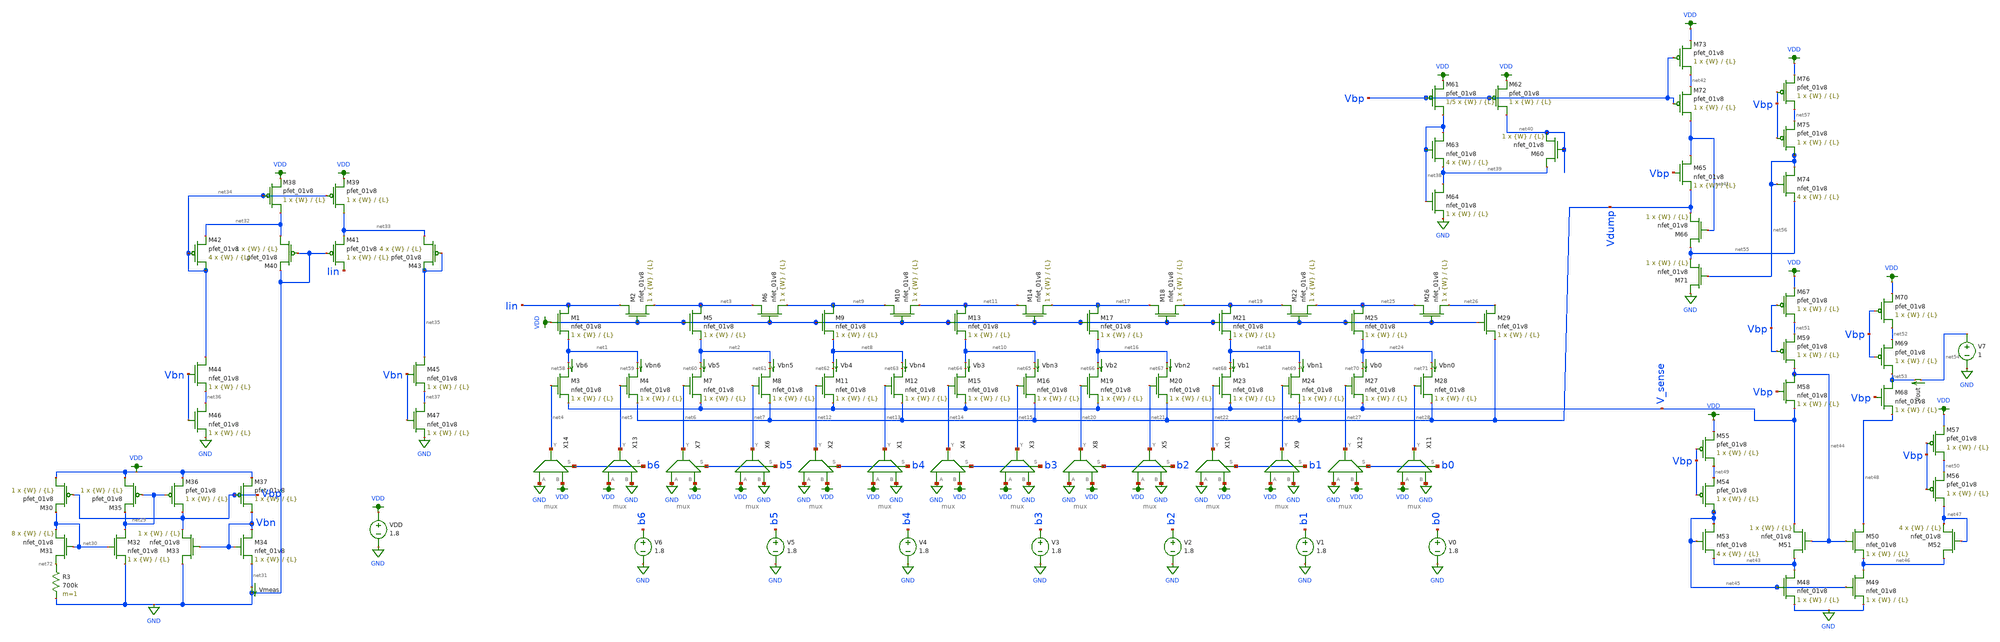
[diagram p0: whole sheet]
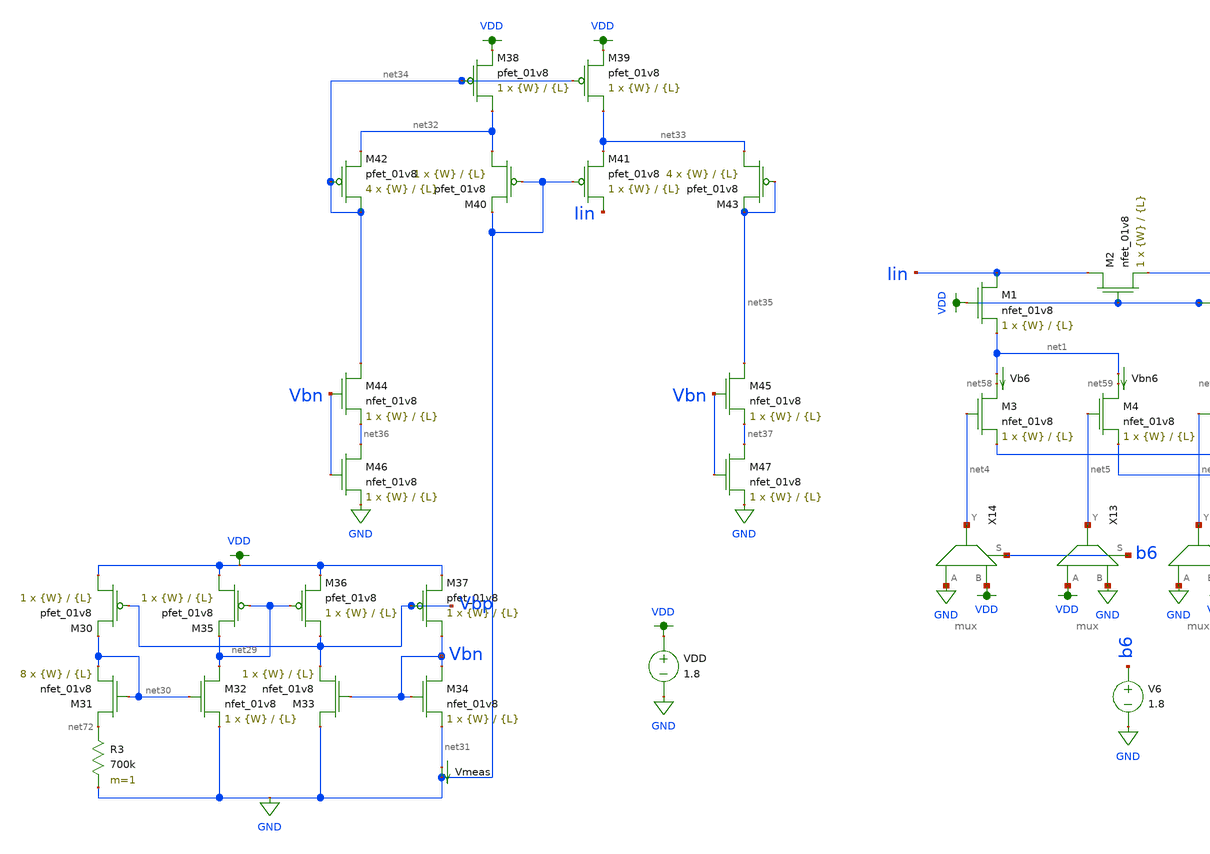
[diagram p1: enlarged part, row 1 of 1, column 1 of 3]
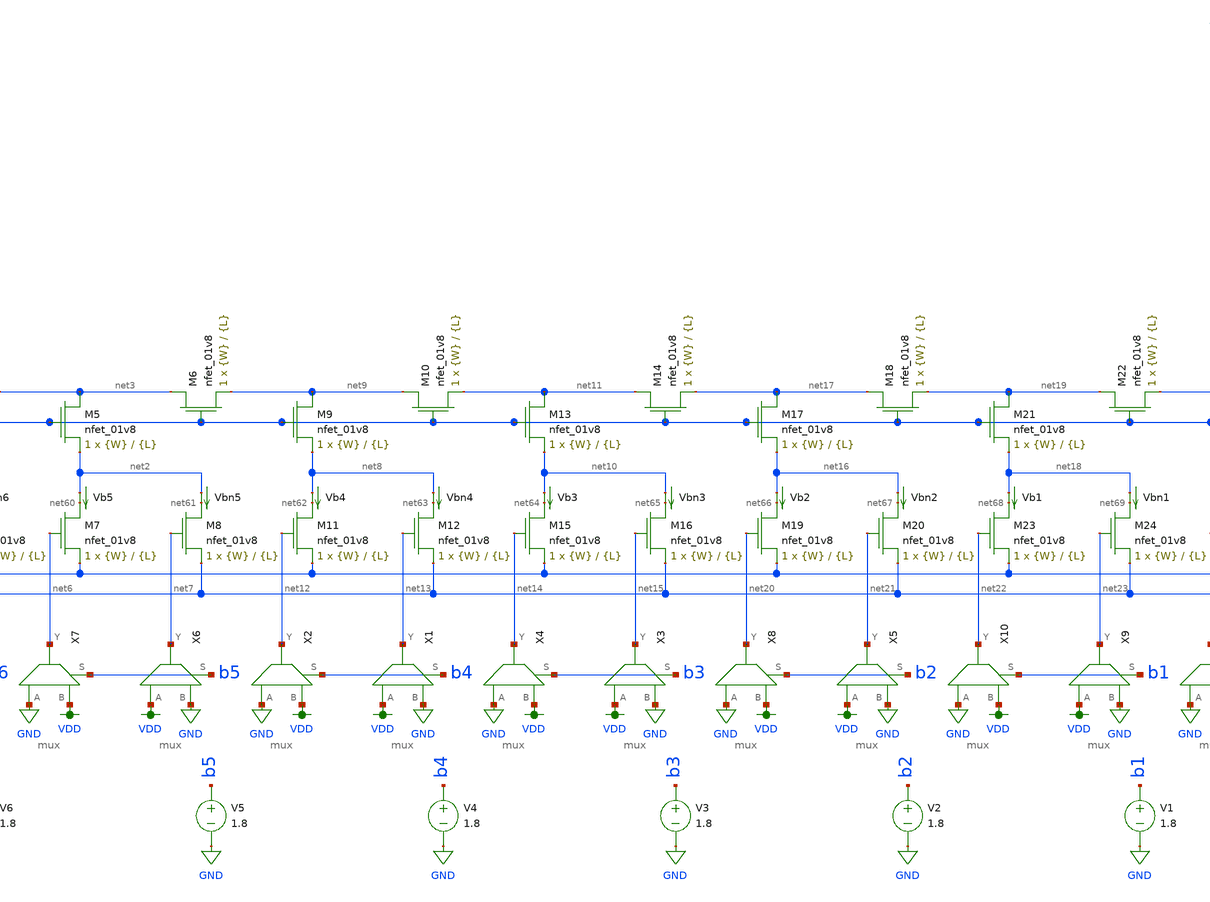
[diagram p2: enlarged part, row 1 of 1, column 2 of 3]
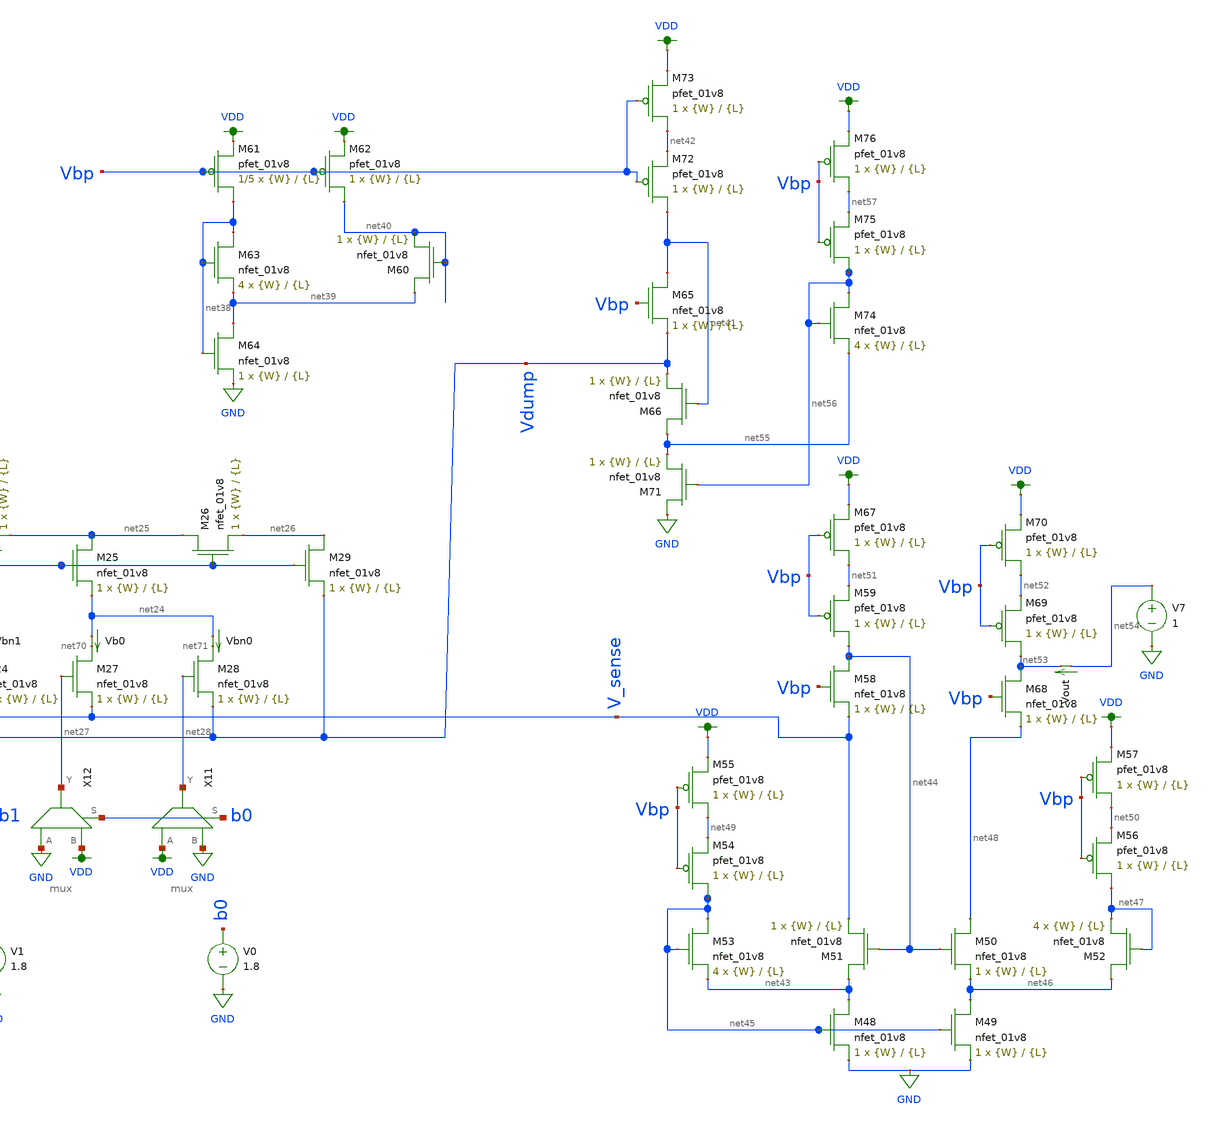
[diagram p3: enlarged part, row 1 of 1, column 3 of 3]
** sch_path: dac/schematics/misc/dac_from_paper.sch
**.subckt dac_from_paper
XM1 Iin VDD net1 GND sky130_fd_pr__nfet_01v8 L={L} W={W} nf=1 ad='int((nf+1)/2) * W/nf * 0.29' as='int((nf+2)/2) * W/nf * 0.29'
+ pd='2*int((nf+1)/2) * (W/nf + 0.29)' ps='2*int((nf+2)/2) * (W/nf + 0.29)' nrd='0.29 / W' nrs='0.29 / W'
+ sa=0 sb=0 sd=0 mult=1 m=1
XM2 Iin VDD net3 GND sky130_fd_pr__nfet_01v8 L={L} W={W} nf=1 ad='int((nf+1)/2) * W/nf * 0.29' as='int((nf+2)/2) * W/nf * 0.29'
+ pd='2*int((nf+1)/2) * (W/nf + 0.29)' ps='2*int((nf+2)/2) * (W/nf + 0.29)' nrd='0.29 / W' nrs='0.29 / W'
+ sa=0 sb=0 sd=0 mult=1 m=1
XM3 net58 net4 V_sense GND sky130_fd_pr__nfet_01v8 L={L} W={W} nf=1 ad='int((nf+1)/2) * W/nf * 0.29'
+ as='int((nf+2)/2) * W/nf * 0.29' pd='2*int((nf+1)/2) * (W/nf + 0.29)' ps='2*int((nf+2)/2) * (W/nf + 0.29)'
+ nrd='0.29 / W' nrs='0.29 / W' sa=0 sb=0 sd=0 mult=1 m=1
XM4 net59 net5 Vdump GND sky130_fd_pr__nfet_01v8 L={L} W={W} nf=1 ad='int((nf+1)/2) * W/nf * 0.29' as='int((nf+2)/2) * W/nf * 0.29'
+ pd='2*int((nf+1)/2) * (W/nf + 0.29)' ps='2*int((nf+2)/2) * (W/nf + 0.29)' nrd='0.29 / W' nrs='0.29 / W'
+ sa=0 sb=0 sd=0 mult=1 m=1
XM5 net3 VDD net2 GND sky130_fd_pr__nfet_01v8 L={L} W={W} nf=1 ad='int((nf+1)/2) * W/nf * 0.29' as='int((nf+2)/2) * W/nf * 0.29'
+ pd='2*int((nf+1)/2) * (W/nf + 0.29)' ps='2*int((nf+2)/2) * (W/nf + 0.29)' nrd='0.29 / W' nrs='0.29 / W'
+ sa=0 sb=0 sd=0 mult=1 m=1
XM6 net3 VDD net9 GND sky130_fd_pr__nfet_01v8 L={L} W={W} nf=1 ad='int((nf+1)/2) * W/nf * 0.29' as='int((nf+2)/2) * W/nf * 0.29'
+ pd='2*int((nf+1)/2) * (W/nf + 0.29)' ps='2*int((nf+2)/2) * (W/nf + 0.29)' nrd='0.29 / W' nrs='0.29 / W'
+ sa=0 sb=0 sd=0 mult=1 m=1
XM7 net60 net6 V_sense GND sky130_fd_pr__nfet_01v8 L={L} W={W} nf=1 ad='int((nf+1)/2) * W/nf * 0.29'
+ as='int((nf+2)/2) * W/nf * 0.29' pd='2*int((nf+1)/2) * (W/nf + 0.29)' ps='2*int((nf+2)/2) * (W/nf + 0.29)'
+ nrd='0.29 / W' nrs='0.29 / W' sa=0 sb=0 sd=0 mult=1 m=1
XM8 net61 net7 Vdump GND sky130_fd_pr__nfet_01v8 L={L} W={W} nf=1 ad='int((nf+1)/2) * W/nf * 0.29' as='int((nf+2)/2) * W/nf * 0.29'
+ pd='2*int((nf+1)/2) * (W/nf + 0.29)' ps='2*int((nf+2)/2) * (W/nf + 0.29)' nrd='0.29 / W' nrs='0.29 / W'
+ sa=0 sb=0 sd=0 mult=1 m=1
XM9 net9 VDD net8 GND sky130_fd_pr__nfet_01v8 L={L} W={W} nf=1 ad='int((nf+1)/2) * W/nf * 0.29' as='int((nf+2)/2) * W/nf * 0.29'
+ pd='2*int((nf+1)/2) * (W/nf + 0.29)' ps='2*int((nf+2)/2) * (W/nf + 0.29)' nrd='0.29 / W' nrs='0.29 / W'
+ sa=0 sb=0 sd=0 mult=1 m=1
XM10 net9 VDD net11 GND sky130_fd_pr__nfet_01v8 L={L} W={W} nf=1 ad='int((nf+1)/2) * W/nf * 0.29' as='int((nf+2)/2) * W/nf * 0.29'
+ pd='2*int((nf+1)/2) * (W/nf + 0.29)' ps='2*int((nf+2)/2) * (W/nf + 0.29)' nrd='0.29 / W' nrs='0.29 / W'
+ sa=0 sb=0 sd=0 mult=1 m=1
XM11 net62 net12 V_sense GND sky130_fd_pr__nfet_01v8 L={L} W={W} nf=1 ad='int((nf+1)/2) * W/nf * 0.29'
+ as='int((nf+2)/2) * W/nf * 0.29' pd='2*int((nf+1)/2) * (W/nf + 0.29)' ps='2*int((nf+2)/2) * (W/nf + 0.29)'
+ nrd='0.29 / W' nrs='0.29 / W' sa=0 sb=0 sd=0 mult=1 m=1
XM12 net63 net13 Vdump GND sky130_fd_pr__nfet_01v8 L={L} W={W} nf=1 ad='int((nf+1)/2) * W/nf * 0.29'
+ as='int((nf+2)/2) * W/nf * 0.29' pd='2*int((nf+1)/2) * (W/nf + 0.29)' ps='2*int((nf+2)/2) * (W/nf + 0.29)'
+ nrd='0.29 / W' nrs='0.29 / W' sa=0 sb=0 sd=0 mult=1 m=1
XM13 net11 VDD net10 GND sky130_fd_pr__nfet_01v8 L={L} W={W} nf=1 ad='int((nf+1)/2) * W/nf * 0.29' as='int((nf+2)/2) * W/nf * 0.29'
+ pd='2*int((nf+1)/2) * (W/nf + 0.29)' ps='2*int((nf+2)/2) * (W/nf + 0.29)' nrd='0.29 / W' nrs='0.29 / W'
+ sa=0 sb=0 sd=0 mult=1 m=1
XM14 net11 VDD net17 GND sky130_fd_pr__nfet_01v8 L={L} W={W} nf=1 ad='int((nf+1)/2) * W/nf * 0.29' as='int((nf+2)/2) * W/nf * 0.29'
+ pd='2*int((nf+1)/2) * (W/nf + 0.29)' ps='2*int((nf+2)/2) * (W/nf + 0.29)' nrd='0.29 / W' nrs='0.29 / W'
+ sa=0 sb=0 sd=0 mult=1 m=1
XM15 net64 net14 V_sense GND sky130_fd_pr__nfet_01v8 L={L} W={W} nf=1 ad='int((nf+1)/2) * W/nf * 0.29'
+ as='int((nf+2)/2) * W/nf * 0.29' pd='2*int((nf+1)/2) * (W/nf + 0.29)' ps='2*int((nf+2)/2) * (W/nf + 0.29)'
+ nrd='0.29 / W' nrs='0.29 / W' sa=0 sb=0 sd=0 mult=1 m=1
XM16 net65 net15 Vdump GND sky130_fd_pr__nfet_01v8 L={L} W={W} nf=1 ad='int((nf+1)/2) * W/nf * 0.29'
+ as='int((nf+2)/2) * W/nf * 0.29' pd='2*int((nf+1)/2) * (W/nf + 0.29)' ps='2*int((nf+2)/2) * (W/nf + 0.29)'
+ nrd='0.29 / W' nrs='0.29 / W' sa=0 sb=0 sd=0 mult=1 m=1
XM17 net17 VDD net16 GND sky130_fd_pr__nfet_01v8 L={L} W={W} nf=1 ad='int((nf+1)/2) * W/nf * 0.29' as='int((nf+2)/2) * W/nf * 0.29'
+ pd='2*int((nf+1)/2) * (W/nf + 0.29)' ps='2*int((nf+2)/2) * (W/nf + 0.29)' nrd='0.29 / W' nrs='0.29 / W'
+ sa=0 sb=0 sd=0 mult=1 m=1
XM18 net17 VDD net19 GND sky130_fd_pr__nfet_01v8 L={L} W={W} nf=1 ad='int((nf+1)/2) * W/nf * 0.29' as='int((nf+2)/2) * W/nf * 0.29'
+ pd='2*int((nf+1)/2) * (W/nf + 0.29)' ps='2*int((nf+2)/2) * (W/nf + 0.29)' nrd='0.29 / W' nrs='0.29 / W'
+ sa=0 sb=0 sd=0 mult=1 m=1
XM19 net66 net20 V_sense GND sky130_fd_pr__nfet_01v8 L={L} W={W} nf=1 ad='int((nf+1)/2) * W/nf * 0.29'
+ as='int((nf+2)/2) * W/nf * 0.29' pd='2*int((nf+1)/2) * (W/nf + 0.29)' ps='2*int((nf+2)/2) * (W/nf + 0.29)'
+ nrd='0.29 / W' nrs='0.29 / W' sa=0 sb=0 sd=0 mult=1 m=1
XM20 net67 net21 Vdump GND sky130_fd_pr__nfet_01v8 L={L} W={W} nf=1 ad='int((nf+1)/2) * W/nf * 0.29'
+ as='int((nf+2)/2) * W/nf * 0.29' pd='2*int((nf+1)/2) * (W/nf + 0.29)' ps='2*int((nf+2)/2) * (W/nf + 0.29)'
+ nrd='0.29 / W' nrs='0.29 / W' sa=0 sb=0 sd=0 mult=1 m=1
XM21 net19 VDD net18 GND sky130_fd_pr__nfet_01v8 L={L} W={W} nf=1 ad='int((nf+1)/2) * W/nf * 0.29' as='int((nf+2)/2) * W/nf * 0.29'
+ pd='2*int((nf+1)/2) * (W/nf + 0.29)' ps='2*int((nf+2)/2) * (W/nf + 0.29)' nrd='0.29 / W' nrs='0.29 / W'
+ sa=0 sb=0 sd=0 mult=1 m=1
XM22 net19 VDD net25 GND sky130_fd_pr__nfet_01v8 L={L} W={W} nf=1 ad='int((nf+1)/2) * W/nf * 0.29' as='int((nf+2)/2) * W/nf * 0.29'
+ pd='2*int((nf+1)/2) * (W/nf + 0.29)' ps='2*int((nf+2)/2) * (W/nf + 0.29)' nrd='0.29 / W' nrs='0.29 / W'
+ sa=0 sb=0 sd=0 mult=1 m=1
XM23 net68 net22 V_sense GND sky130_fd_pr__nfet_01v8 L={L} W={W} nf=1 ad='int((nf+1)/2) * W/nf * 0.29'
+ as='int((nf+2)/2) * W/nf * 0.29' pd='2*int((nf+1)/2) * (W/nf + 0.29)' ps='2*int((nf+2)/2) * (W/nf + 0.29)'
+ nrd='0.29 / W' nrs='0.29 / W' sa=0 sb=0 sd=0 mult=1 m=1
XM24 net69 net23 Vdump GND sky130_fd_pr__nfet_01v8 L={L} W={W} nf=1 ad='int((nf+1)/2) * W/nf * 0.29'
+ as='int((nf+2)/2) * W/nf * 0.29' pd='2*int((nf+1)/2) * (W/nf + 0.29)' ps='2*int((nf+2)/2) * (W/nf + 0.29)'
+ nrd='0.29 / W' nrs='0.29 / W' sa=0 sb=0 sd=0 mult=1 m=1
XM25 net25 VDD net24 GND sky130_fd_pr__nfet_01v8 L={L} W={W} nf=1 ad='int((nf+1)/2) * W/nf * 0.29' as='int((nf+2)/2) * W/nf * 0.29'
+ pd='2*int((nf+1)/2) * (W/nf + 0.29)' ps='2*int((nf+2)/2) * (W/nf + 0.29)' nrd='0.29 / W' nrs='0.29 / W'
+ sa=0 sb=0 sd=0 mult=1 m=1
XM26 net25 VDD net26 GND sky130_fd_pr__nfet_01v8 L={L} W={W} nf=1 ad='int((nf+1)/2) * W/nf * 0.29' as='int((nf+2)/2) * W/nf * 0.29'
+ pd='2*int((nf+1)/2) * (W/nf + 0.29)' ps='2*int((nf+2)/2) * (W/nf + 0.29)' nrd='0.29 / W' nrs='0.29 / W'
+ sa=0 sb=0 sd=0 mult=1 m=1
XM27 net70 net27 V_sense GND sky130_fd_pr__nfet_01v8 L={L} W={W} nf=1 ad='int((nf+1)/2) * W/nf * 0.29'
+ as='int((nf+2)/2) * W/nf * 0.29' pd='2*int((nf+1)/2) * (W/nf + 0.29)' ps='2*int((nf+2)/2) * (W/nf + 0.29)'
+ nrd='0.29 / W' nrs='0.29 / W' sa=0 sb=0 sd=0 mult=1 m=1
XM28 net71 net28 Vdump GND sky130_fd_pr__nfet_01v8 L={L} W={W} nf=1 ad='int((nf+1)/2) * W/nf * 0.29'
+ as='int((nf+2)/2) * W/nf * 0.29' pd='2*int((nf+1)/2) * (W/nf + 0.29)' ps='2*int((nf+2)/2) * (W/nf + 0.29)'
+ nrd='0.29 / W' nrs='0.29 / W' sa=0 sb=0 sd=0 mult=1 m=1
XM29 net26 VDD Vdump GND sky130_fd_pr__nfet_01v8 L={L} W={W} nf=1 ad='int((nf+1)/2) * W/nf * 0.29' as='int((nf+2)/2) * W/nf * 0.29'
+ pd='2*int((nf+1)/2) * (W/nf + 0.29)' ps='2*int((nf+2)/2) * (W/nf + 0.29)' nrd='0.29 / W' nrs='0.29 / W'
+ sa=0 sb=0 sd=0 mult=1 m=1
Vb0 net24 net70 0
.save i(vb0)
Vbn0 net24 net71 0
.save i(vbn0)
Vb5 net2 net60 0
.save i(vb5)
Vb6 net1 net58 0
.save i(vb6)
Vb1 net18 net68 0
.save i(vb1)
Vb2 net16 net66 0
.save i(vb2)
Vb3 net10 net64 0
.save i(vb3)
Vb4 net8 net62 0
.save i(vb4)
Vbn1 net18 net69 0
.save i(vbn1)
Vbn2 net16 net67 0
.save i(vbn2)
Vbn3 net10 net65 0
.save i(vbn3)
Vbn4 net8 net63 0
.save i(vbn4)
Vbn5 net2 net61 0
.save i(vbn5)
Vbn6 net1 net59 0
.save i(vbn6)
V0 b0 GND 1.8
V1 b1 GND 1.8
V2 b2 GND 1.8
V3 b3 GND 1.8
V4 b4 GND 1.8
V5 b5 GND 1.8
V6 b6 GND 1.8
XM30 VDD Vbp net30 VDD sky130_fd_pr__pfet_01v8 L={L} W={W} nf=1 ad='int((nf+1)/2) * W/nf * 0.29' as='int((nf+2)/2) * W/nf * 0.29'
+ pd='2*int((nf+1)/2) * (W/nf + 0.29)' ps='2*int((nf+2)/2) * (W/nf + 0.29)' nrd='0.29 / W' nrs='0.29 / W'
+ sa=0 sb=0 sd=0 mult=1 m=1
XM31 net72 net30 net30 GND sky130_fd_pr__nfet_01v8 L={L} W={W} nf=1 ad='int((nf+1)/2) * W/nf * 0.29'
+ as='int((nf+2)/2) * W/nf * 0.29' pd='2*int((nf+1)/2) * (W/nf + 0.29)' ps='2*int((nf+2)/2) * (W/nf + 0.29)'
+ nrd='0.29 / W' nrs='0.29 / W' sa=0 sb=0 sd=0 mult=8 m=8
R3 net72 GND 700k m=1
XM32 net29 net30 GND GND sky130_fd_pr__nfet_01v8 L={L} W={W} nf=1 ad='int((nf+1)/2) * W/nf * 0.29' as='int((nf+2)/2) * W/nf * 0.29'
+ pd='2*int((nf+1)/2) * (W/nf + 0.29)' ps='2*int((nf+2)/2) * (W/nf + 0.29)' nrd='0.29 / W' nrs='0.29 / W'
+ sa=0 sb=0 sd=0 mult=1 m=1
XM33 GND Vbn Vbp GND sky130_fd_pr__nfet_01v8 L={L} W={W} nf=1 ad='int((nf+1)/2) * W/nf * 0.29' as='int((nf+2)/2) * W/nf * 0.29'
+ pd='2*int((nf+1)/2) * (W/nf + 0.29)' ps='2*int((nf+2)/2) * (W/nf + 0.29)' nrd='0.29 / W' nrs='0.29 / W'
+ sa=0 sb=0 sd=0 mult=1 m=1
XM34 Vbn Vbn net31 GND sky130_fd_pr__nfet_01v8 L={L} W={W} nf=1 ad='int((nf+1)/2) * W/nf * 0.29' as='int((nf+2)/2) * W/nf * 0.29'
+ pd='2*int((nf+1)/2) * (W/nf + 0.29)' ps='2*int((nf+2)/2) * (W/nf + 0.29)' nrd='0.29 / W' nrs='0.29 / W'
+ sa=0 sb=0 sd=0 mult=1 m=1
XM35 VDD net29 net29 VDD sky130_fd_pr__pfet_01v8 L={L} W={W} nf=1 ad='int((nf+1)/2) * W/nf * 0.29' as='int((nf+2)/2) * W/nf * 0.29'
+ pd='2*int((nf+1)/2) * (W/nf + 0.29)' ps='2*int((nf+2)/2) * (W/nf + 0.29)' nrd='0.29 / W' nrs='0.29 / W'
+ sa=0 sb=0 sd=0 mult=1 m=1
XM36 Vbp net29 VDD VDD sky130_fd_pr__pfet_01v8 L={L} W={W} nf=1 ad='int((nf+1)/2) * W/nf * 0.29' as='int((nf+2)/2) * W/nf * 0.29'
+ pd='2*int((nf+1)/2) * (W/nf + 0.29)' ps='2*int((nf+2)/2) * (W/nf + 0.29)' nrd='0.29 / W' nrs='0.29 / W'
+ sa=0 sb=0 sd=0 mult=1 m=1
XM37 Vbn Vbp VDD VDD sky130_fd_pr__pfet_01v8 L={L} W={W} nf=1 ad='int((nf+1)/2) * W/nf * 0.29' as='int((nf+2)/2) * W/nf * 0.29'
+ pd='2*int((nf+1)/2) * (W/nf + 0.29)' ps='2*int((nf+2)/2) * (W/nf + 0.29)' nrd='0.29 / W' nrs='0.29 / W'
+ sa=0 sb=0 sd=0 mult=1 m=1
VDD VDD GND 1.8
Vmeas net31 GND 0
.save i(vmeas)
X13 VDD GND net5 b6 mux
X14 GND VDD net4 b6 mux
X6 VDD GND net7 b5 mux
X7 GND VDD net6 b5 mux
X1 VDD GND net13 b4 mux
X2 GND VDD net12 b4 mux
X3 VDD GND net15 b3 mux
X4 GND VDD net14 b3 mux
X5 VDD GND net21 b2 mux
X8 GND VDD net20 b2 mux
X9 VDD GND net23 b1 mux
X10 GND VDD net22 b1 mux
X11 VDD GND net28 b0 mux
X12 GND VDD net27 b0 mux
XM38 net32 net34 VDD VDD sky130_fd_pr__pfet_01v8 L={L} W={W} nf=1 ad='int((nf+1)/2) * W/nf * 0.29' as='int((nf+2)/2) * W/nf * 0.29'
+ pd='2*int((nf+1)/2) * (W/nf + 0.29)' ps='2*int((nf+2)/2) * (W/nf + 0.29)' nrd='0.29 / W' nrs='0.29 / W'
+ sa=0 sb=0 sd=0 mult=1 m=1
XM39 net33 net34 VDD VDD sky130_fd_pr__pfet_01v8 L={L} W={W} nf=1 ad='int((nf+1)/2) * W/nf * 0.29' as='int((nf+2)/2) * W/nf * 0.29'
+ pd='2*int((nf+1)/2) * (W/nf + 0.29)' ps='2*int((nf+2)/2) * (W/nf + 0.29)' nrd='0.29 / W' nrs='0.29 / W'
+ sa=0 sb=0 sd=0 mult=1 m=1
XM40 net32 GND GND VDD sky130_fd_pr__pfet_01v8 L={L} W={W} nf=1 ad='int((nf+1)/2) * W/nf * 0.29' as='int((nf+2)/2) * W/nf * 0.29'
+ pd='2*int((nf+1)/2) * (W/nf + 0.29)' ps='2*int((nf+2)/2) * (W/nf + 0.29)' nrd='0.29 / W' nrs='0.29 / W'
+ sa=0 sb=0 sd=0 mult=1 m=1
XM41 Iin GND net33 VDD sky130_fd_pr__pfet_01v8 L={L} W={W} nf=1 ad='int((nf+1)/2) * W/nf * 0.29' as='int((nf+2)/2) * W/nf * 0.29'
+ pd='2*int((nf+1)/2) * (W/nf + 0.29)' ps='2*int((nf+2)/2) * (W/nf + 0.29)' nrd='0.29 / W' nrs='0.29 / W'
+ sa=0 sb=0 sd=0 mult=1 m=1
XM42 net34 net34 net32 VDD sky130_fd_pr__pfet_01v8 L={L} W={W} nf=1 ad='int((nf+1)/2) * W/nf * 0.29'
+ as='int((nf+2)/2) * W/nf * 0.29' pd='2*int((nf+1)/2) * (W/nf + 0.29)' ps='2*int((nf+2)/2) * (W/nf + 0.29)'
+ nrd='0.29 / W' nrs='0.29 / W' sa=0 sb=0 sd=0 mult=4 m=4
XM43 net33 net35 net35 VDD sky130_fd_pr__pfet_01v8 L={L} W={W} nf=1 ad='int((nf+1)/2) * W/nf * 0.29'
+ as='int((nf+2)/2) * W/nf * 0.29' pd='2*int((nf+1)/2) * (W/nf + 0.29)' ps='2*int((nf+2)/2) * (W/nf + 0.29)'
+ nrd='0.29 / W' nrs='0.29 / W' sa=0 sb=0 sd=0 mult=4 m=4
XM44 net34 Vbn net36 GND sky130_fd_pr__nfet_01v8 L={L} W={W} nf=1 ad='int((nf+1)/2) * W/nf * 0.29' as='int((nf+2)/2) * W/nf * 0.29'
+ pd='2*int((nf+1)/2) * (W/nf + 0.29)' ps='2*int((nf+2)/2) * (W/nf + 0.29)' nrd='0.29 / W' nrs='0.29 / W'
+ sa=0 sb=0 sd=0 mult=1 m=1
XM45 net35 Vbn net37 GND sky130_fd_pr__nfet_01v8 L={L} W={W} nf=1 ad='int((nf+1)/2) * W/nf * 0.29' as='int((nf+2)/2) * W/nf * 0.29'
+ pd='2*int((nf+1)/2) * (W/nf + 0.29)' ps='2*int((nf+2)/2) * (W/nf + 0.29)' nrd='0.29 / W' nrs='0.29 / W'
+ sa=0 sb=0 sd=0 mult=1 m=1
XM46 net36 Vbn GND GND sky130_fd_pr__nfet_01v8 L={L} W={W} nf=1 ad='int((nf+1)/2) * W/nf * 0.29' as='int((nf+2)/2) * W/nf * 0.29'
+ pd='2*int((nf+1)/2) * (W/nf + 0.29)' ps='2*int((nf+2)/2) * (W/nf + 0.29)' nrd='0.29 / W' nrs='0.29 / W'
+ sa=0 sb=0 sd=0 mult=1 m=1
XM47 net37 Vbn GND GND sky130_fd_pr__nfet_01v8 L={L} W={W} nf=1 ad='int((nf+1)/2) * W/nf * 0.29' as='int((nf+2)/2) * W/nf * 0.29'
+ pd='2*int((nf+1)/2) * (W/nf + 0.29)' ps='2*int((nf+2)/2) * (W/nf + 0.29)' nrd='0.29 / W' nrs='0.29 / W'
+ sa=0 sb=0 sd=0 mult=1 m=1
XM60 net39 net40 net40 GND sky130_fd_pr__nfet_01v8 L={L} W={W} nf=1 ad='int((nf+1)/2) * W/nf * 0.29'
+ as='int((nf+2)/2) * W/nf * 0.29' pd='2*int((nf+1)/2) * (W/nf + 0.29)' ps='2*int((nf+2)/2) * (W/nf + 0.29)'
+ nrd='0.29 / W' nrs='0.29 / W' sa=0 sb=0 sd=0 mult=1 m=1
XM61 net38 Vbp VDD VDD sky130_fd_pr__pfet_01v8 L={L} W={W} nf=1 ad='int((nf+1)/2) * W/nf * 0.29' as='int((nf+2)/2) * W/nf * 0.29'
+ pd='2*int((nf+1)/2) * (W/nf + 0.29)' ps='2*int((nf+2)/2) * (W/nf + 0.29)' nrd='0.29 / W' nrs='0.29 / W'
+ sa=0 sb=0 sd=0 mult=1/5 m=1/5
XM62 net40 Vbp VDD VDD sky130_fd_pr__pfet_01v8 L={L} W={W} nf=1 ad='int((nf+1)/2) * W/nf * 0.29' as='int((nf+2)/2) * W/nf * 0.29'
+ pd='2*int((nf+1)/2) * (W/nf + 0.29)' ps='2*int((nf+2)/2) * (W/nf + 0.29)' nrd='0.29 / W' nrs='0.29 / W'
+ sa=0 sb=0 sd=0 mult=1 m=1
XM63 net38 net38 net39 GND sky130_fd_pr__nfet_01v8 L={L} W={W} nf=1 ad='int((nf+1)/2) * W/nf * 0.29'
+ as='int((nf+2)/2) * W/nf * 0.29' pd='2*int((nf+1)/2) * (W/nf + 0.29)' ps='2*int((nf+2)/2) * (W/nf + 0.29)'
+ nrd='0.29 / W' nrs='0.29 / W' sa=0 sb=0 sd=0 mult=4 m=4
XM64 net39 net38 GND GND sky130_fd_pr__nfet_01v8 L={L} W={W} nf=1 ad='int((nf+1)/2) * W/nf * 0.29' as='int((nf+2)/2) * W/nf * 0.29'
+ pd='2*int((nf+1)/2) * (W/nf + 0.29)' ps='2*int((nf+2)/2) * (W/nf + 0.29)' nrd='0.29 / W' nrs='0.29 / W'
+ sa=0 sb=0 sd=0 mult=1 m=1
XM65 net41 Vbp Vdump GND sky130_fd_pr__nfet_01v8 L={L} W={W} nf=1 ad='int((nf+1)/2) * W/nf * 0.29' as='int((nf+2)/2) * W/nf * 0.29'
+ pd='2*int((nf+1)/2) * (W/nf + 0.29)' ps='2*int((nf+2)/2) * (W/nf + 0.29)' nrd='0.29 / W' nrs='0.29 / W'
+ sa=0 sb=0 sd=0 mult=1 m=1
XM66 net55 net41 Vdump GND sky130_fd_pr__nfet_01v8 L={L} W={W} nf=1 ad='int((nf+1)/2) * W/nf * 0.29'
+ as='int((nf+2)/2) * W/nf * 0.29' pd='2*int((nf+1)/2) * (W/nf + 0.29)' ps='2*int((nf+2)/2) * (W/nf + 0.29)'
+ nrd='0.29 / W' nrs='0.29 / W' sa=0 sb=0 sd=0 mult=1 m=1
XM72 net41 Vbp net42 VDD sky130_fd_pr__pfet_01v8 L={L} W={W} nf=1 ad='int((nf+1)/2) * W/nf * 0.29' as='int((nf+2)/2) * W/nf * 0.29'
+ pd='2*int((nf+1)/2) * (W/nf + 0.29)' ps='2*int((nf+2)/2) * (W/nf + 0.29)' nrd='0.29 / W' nrs='0.29 / W'
+ sa=0 sb=0 sd=0 mult=1 m=1
XM73 net42 Vbp VDD VDD sky130_fd_pr__pfet_01v8 L={L} W={W} nf=1 ad='int((nf+1)/2) * W/nf * 0.29' as='int((nf+2)/2) * W/nf * 0.29'
+ pd='2*int((nf+1)/2) * (W/nf + 0.29)' ps='2*int((nf+2)/2) * (W/nf + 0.29)' nrd='0.29 / W' nrs='0.29 / W'
+ sa=0 sb=0 sd=0 mult=1 m=1
Vout net54 net53 0
.save i(vout)
V7 net54 GND 1
XM48 net43 net45 GND GND sky130_fd_pr__nfet_01v8 L={L} W={W} nf=1 ad='int((nf+1)/2) * W/nf * 0.29' as='int((nf+2)/2) * W/nf * 0.29'
+ pd='2*int((nf+1)/2) * (W/nf + 0.29)' ps='2*int((nf+2)/2) * (W/nf + 0.29)' nrd='0.29 / W' nrs='0.29 / W'
+ sa=0 sb=0 sd=0 mult=1 m=1
XM49 net46 net45 GND GND sky130_fd_pr__nfet_01v8 L={L} W={W} nf=1 ad='int((nf+1)/2) * W/nf * 0.29' as='int((nf+2)/2) * W/nf * 0.29'
+ pd='2*int((nf+1)/2) * (W/nf + 0.29)' ps='2*int((nf+2)/2) * (W/nf + 0.29)' nrd='0.29 / W' nrs='0.29 / W'
+ sa=0 sb=0 sd=0 mult=1 m=1
XM50 net48 net44 net46 GND sky130_fd_pr__nfet_01v8 L={L} W={W} nf=1 ad='int((nf+1)/2) * W/nf * 0.29'
+ as='int((nf+2)/2) * W/nf * 0.29' pd='2*int((nf+1)/2) * (W/nf + 0.29)' ps='2*int((nf+2)/2) * (W/nf + 0.29)'
+ nrd='0.29 / W' nrs='0.29 / W' sa=0 sb=0 sd=0 mult=1 m=1
XM51 net43 net44 V_sense GND sky130_fd_pr__nfet_01v8 L={L} W={W} nf=1 ad='int((nf+1)/2) * W/nf * 0.29'
+ as='int((nf+2)/2) * W/nf * 0.29' pd='2*int((nf+1)/2) * (W/nf + 0.29)' ps='2*int((nf+2)/2) * (W/nf + 0.29)'
+ nrd='0.29 / W' nrs='0.29 / W' sa=0 sb=0 sd=0 mult=1 m=1
XM52 net46 net47 net47 GND sky130_fd_pr__nfet_01v8 L={L} W={W} nf=1 ad='int((nf+1)/2) * W/nf * 0.29'
+ as='int((nf+2)/2) * W/nf * 0.29' pd='2*int((nf+1)/2) * (W/nf + 0.29)' ps='2*int((nf+2)/2) * (W/nf + 0.29)'
+ nrd='0.29 / W' nrs='0.29 / W' sa=0 sb=0 sd=0 mult=4 m=4
XM53 net45 net45 net43 GND sky130_fd_pr__nfet_01v8 L={L} W={W} nf=1 ad='int((nf+1)/2) * W/nf * 0.29'
+ as='int((nf+2)/2) * W/nf * 0.29' pd='2*int((nf+1)/2) * (W/nf + 0.29)' ps='2*int((nf+2)/2) * (W/nf + 0.29)'
+ nrd='0.29 / W' nrs='0.29 / W' sa=0 sb=0 sd=0 mult=4 m=4
XM54 net45 Vbp net49 VDD sky130_fd_pr__pfet_01v8 L={L} W={W} nf=1 ad='int((nf+1)/2) * W/nf * 0.29' as='int((nf+2)/2) * W/nf * 0.29'
+ pd='2*int((nf+1)/2) * (W/nf + 0.29)' ps='2*int((nf+2)/2) * (W/nf + 0.29)' nrd='0.29 / W' nrs='0.29 / W'
+ sa=0 sb=0 sd=0 mult=1 m=1
XM55 net49 Vbp VDD VDD sky130_fd_pr__pfet_01v8 L={L} W={W} nf=1 ad='int((nf+1)/2) * W/nf * 0.29' as='int((nf+2)/2) * W/nf * 0.29'
+ pd='2*int((nf+1)/2) * (W/nf + 0.29)' ps='2*int((nf+2)/2) * (W/nf + 0.29)' nrd='0.29 / W' nrs='0.29 / W'
+ sa=0 sb=0 sd=0 mult=1 m=1
XM56 net47 Vbp net50 VDD sky130_fd_pr__pfet_01v8 L={L} W={W} nf=1 ad='int((nf+1)/2) * W/nf * 0.29' as='int((nf+2)/2) * W/nf * 0.29'
+ pd='2*int((nf+1)/2) * (W/nf + 0.29)' ps='2*int((nf+2)/2) * (W/nf + 0.29)' nrd='0.29 / W' nrs='0.29 / W'
+ sa=0 sb=0 sd=0 mult=1 m=1
XM57 net50 Vbp VDD VDD sky130_fd_pr__pfet_01v8 L={L} W={W} nf=1 ad='int((nf+1)/2) * W/nf * 0.29' as='int((nf+2)/2) * W/nf * 0.29'
+ pd='2*int((nf+1)/2) * (W/nf + 0.29)' ps='2*int((nf+2)/2) * (W/nf + 0.29)' nrd='0.29 / W' nrs='0.29 / W'
+ sa=0 sb=0 sd=0 mult=1 m=1
XM58 net44 Vbp V_sense GND sky130_fd_pr__nfet_01v8 L={L} W={W} nf=1 ad='int((nf+1)/2) * W/nf * 0.29'
+ as='int((nf+2)/2) * W/nf * 0.29' pd='2*int((nf+1)/2) * (W/nf + 0.29)' ps='2*int((nf+2)/2) * (W/nf + 0.29)'
+ nrd='0.29 / W' nrs='0.29 / W' sa=0 sb=0 sd=0 mult=1 m=1
XM59 net44 Vbp net51 VDD sky130_fd_pr__pfet_01v8 L={L} W={W} nf=1 ad='int((nf+1)/2) * W/nf * 0.29' as='int((nf+2)/2) * W/nf * 0.29'
+ pd='2*int((nf+1)/2) * (W/nf + 0.29)' ps='2*int((nf+2)/2) * (W/nf + 0.29)' nrd='0.29 / W' nrs='0.29 / W'
+ sa=0 sb=0 sd=0 mult=1 m=1
XM67 net51 Vbp VDD VDD sky130_fd_pr__pfet_01v8 L={L} W={W} nf=1 ad='int((nf+1)/2) * W/nf * 0.29' as='int((nf+2)/2) * W/nf * 0.29'
+ pd='2*int((nf+1)/2) * (W/nf + 0.29)' ps='2*int((nf+2)/2) * (W/nf + 0.29)' nrd='0.29 / W' nrs='0.29 / W'
+ sa=0 sb=0 sd=0 mult=1 m=1
XM68 net53 Vbp net48 GND sky130_fd_pr__nfet_01v8 L={L} W={W} nf=1 ad='int((nf+1)/2) * W/nf * 0.29' as='int((nf+2)/2) * W/nf * 0.29'
+ pd='2*int((nf+1)/2) * (W/nf + 0.29)' ps='2*int((nf+2)/2) * (W/nf + 0.29)' nrd='0.29 / W' nrs='0.29 / W'
+ sa=0 sb=0 sd=0 mult=1 m=1
XM69 net53 Vbp net52 VDD sky130_fd_pr__pfet_01v8 L={L} W={W} nf=1 ad='int((nf+1)/2) * W/nf * 0.29' as='int((nf+2)/2) * W/nf * 0.29'
+ pd='2*int((nf+1)/2) * (W/nf + 0.29)' ps='2*int((nf+2)/2) * (W/nf + 0.29)' nrd='0.29 / W' nrs='0.29 / W'
+ sa=0 sb=0 sd=0 mult=1 m=1
XM70 net52 Vbp VDD VDD sky130_fd_pr__pfet_01v8 L={L} W={W} nf=1 ad='int((nf+1)/2) * W/nf * 0.29' as='int((nf+2)/2) * W/nf * 0.29'
+ pd='2*int((nf+1)/2) * (W/nf + 0.29)' ps='2*int((nf+2)/2) * (W/nf + 0.29)' nrd='0.29 / W' nrs='0.29 / W'
+ sa=0 sb=0 sd=0 mult=1 m=1
XM71 GND net56 net55 GND sky130_fd_pr__nfet_01v8 L={L} W={W} nf=1 ad='int((nf+1)/2) * W/nf * 0.29' as='int((nf+2)/2) * W/nf * 0.29'
+ pd='2*int((nf+1)/2) * (W/nf + 0.29)' ps='2*int((nf+2)/2) * (W/nf + 0.29)' nrd='0.29 / W' nrs='0.29 / W'
+ sa=0 sb=0 sd=0 mult=1 m=1
XM74 net56 net56 net55 GND sky130_fd_pr__nfet_01v8 L={L} W={W} nf=1 ad='int((nf+1)/2) * W/nf * 0.29'
+ as='int((nf+2)/2) * W/nf * 0.29' pd='2*int((nf+1)/2) * (W/nf + 0.29)' ps='2*int((nf+2)/2) * (W/nf + 0.29)'
+ nrd='0.29 / W' nrs='0.29 / W' sa=0 sb=0 sd=0 mult=4 m=4
XM75 net56 Vbp net57 VDD sky130_fd_pr__pfet_01v8 L={L} W={W} nf=1 ad='int((nf+1)/2) * W/nf * 0.29' as='int((nf+2)/2) * W/nf * 0.29'
+ pd='2*int((nf+1)/2) * (W/nf + 0.29)' ps='2*int((nf+2)/2) * (W/nf + 0.29)' nrd='0.29 / W' nrs='0.29 / W'
+ sa=0 sb=0 sd=0 mult=1 m=1
XM76 net57 Vbp VDD VDD sky130_fd_pr__pfet_01v8 L={L} W={W} nf=1 ad='int((nf+1)/2) * W/nf * 0.29' as='int((nf+2)/2) * W/nf * 0.29'
+ pd='2*int((nf+1)/2) * (W/nf + 0.29)' ps='2*int((nf+2)/2) * (W/nf + 0.29)' nrd='0.29 / W' nrs='0.29 / W'
+ sa=0 sb=0 sd=0 mult=1 m=1
**** begin user architecture code

.option wnflag=1
.param MC_SWITCH=1.0
.lib ~/skywater/skywater-pdk/libraries/sky130_fd_pr_ngspice/latest/models/sky130.lib.spice tt


.param W=32
.param L=4
.control
set wr_vecnames
set wr_singlescale
let code = 0
  while code < 128
    if code eq 0
      let b0 = 0
    else
      let b0 = code % 2
    end
    if floor(code / 2) eq 0
      let b1 = 0
    else
      let b1 = floor(code / 2) % 2
    end
    if floor(code / 4) eq 0
      let b2 = 0
    else
      let b2 = floor(code / 4) % 2
    end
    if floor(code / 8) eq 0
      let b3 = 0
    else
      let b3 = floor(code / 8) % 2
    end
    if floor(code / 16) eq 0
      let b4 = 0
    else
      let b4 = floor(code / 16) % 2
    end
    if floor(code / 32) eq 0
      let b5 = 0
    else
      let b5 = floor(code / 32) % 2
    end
    if floor(code / 64) eq 0
      let b6 = 0
    else
      let b6 = floor(code / 64) % 2
    end
    alter v0 $&b0
    alter v1 $&b1
    alter v2 $&b2
    alter v3 $&b3
    alter v4 $&b4
    alter v5 $&b5
    alter v6 $&b6
    save all
    op
    wrdata ~/Documents/current-output-dac-vlsi/simulations/dac_paper_sim.txt i(Vmeas) i(vb0) i(vb1)
+ i(vb2) i(vb3) i(vb4) i(vb5) i(vb6) i(Vout) v(V_sense) v(Vdump)
    if code eq 0
      set appendwrite
      set wr_vecnames = FALSE
    end
    let code = code + 1
  end
.endc

**** end user architecture code
**.ends

* expanding   symbol:  /home/madvlsi/Documents/current-output-dac-vlsi/schematics/mux.sym # of
*+ pins=4
** sym_path: dac/schematics/mux.sym
** sch_path: dac/schematics/mux.sch
.subckt mux A B Y S
*.ipin A
*.ipin B
*.ipin S
*.opin Y
XM1 A S Y VDD sky130_fd_pr__pfet_01v8 L=0.15 W=1 nf=1 ad='int((nf+1)/2) * W/nf * 0.29' as='int((nf+2)/2) * W/nf * 0.29'
+ pd='2*int((nf+1)/2) * (W/nf + 0.29)' ps='2*int((nf+2)/2) * (W/nf + 0.29)' nrd='0.29 / W' nrs='0.29 / W'
+ sa=0 sb=0 sd=0 mult=1 m=1
XM3 net1 S VDD VDD sky130_fd_pr__pfet_01v8 L=0.15 W=1 nf=1 ad='int((nf+1)/2) * W/nf * 0.29' as='int((nf+2)/2) * W/nf * 0.29'
+ pd='2*int((nf+1)/2) * (W/nf + 0.29)' ps='2*int((nf+2)/2) * (W/nf + 0.29)' nrd='0.29 / W' nrs='0.29 / W'
+ sa=0 sb=0 sd=0 mult=1 m=1
XM4 net1 S GND GND sky130_fd_pr__nfet_01v8 L=0.15 W=1 nf=1 ad='int((nf+1)/2) * W/nf * 0.29' as='int((nf+2)/2) * W/nf * 0.29'
+ pd='2*int((nf+1)/2) * (W/nf + 0.29)' ps='2*int((nf+2)/2) * (W/nf + 0.29)' nrd='0.29 / W' nrs='0.29 / W'
+ sa=0 sb=0 sd=0 mult=1 m=1
XM5 A net1 Y GND sky130_fd_pr__nfet_01v8 L=0.15 W=1 nf=1 ad='int((nf+1)/2) * W/nf * 0.29' as='int((nf+2)/2) * W/nf * 0.29'
+ pd='2*int((nf+1)/2) * (W/nf + 0.29)' ps='2*int((nf+2)/2) * (W/nf + 0.29)' nrd='0.29 / W' nrs='0.29 / W'
+ sa=0 sb=0 sd=0 mult=1 m=1
XM2 B net1 Y VDD sky130_fd_pr__pfet_01v8 L=0.15 W=1 nf=1 ad='int((nf+1)/2) * W/nf * 0.29' as='int((nf+2)/2) * W/nf * 0.29'
+ pd='2*int((nf+1)/2) * (W/nf + 0.29)' ps='2*int((nf+2)/2) * (W/nf + 0.29)' nrd='0.29 / W' nrs='0.29 / W'
+ sa=0 sb=0 sd=0 mult=1 m=1
XM6 B S Y GND sky130_fd_pr__nfet_01v8 L=0.15 W=1 nf=1 ad='int((nf+1)/2) * W/nf * 0.29' as='int((nf+2)/2) * W/nf * 0.29'
+ pd='2*int((nf+1)/2) * (W/nf + 0.29)' ps='2*int((nf+2)/2) * (W/nf + 0.29)' nrd='0.29 / W' nrs='0.29 / W'
+ sa=0 sb=0 sd=0 mult=1 m=1
.ends

.GLOBAL GND
.GLOBAL VDD
.end
